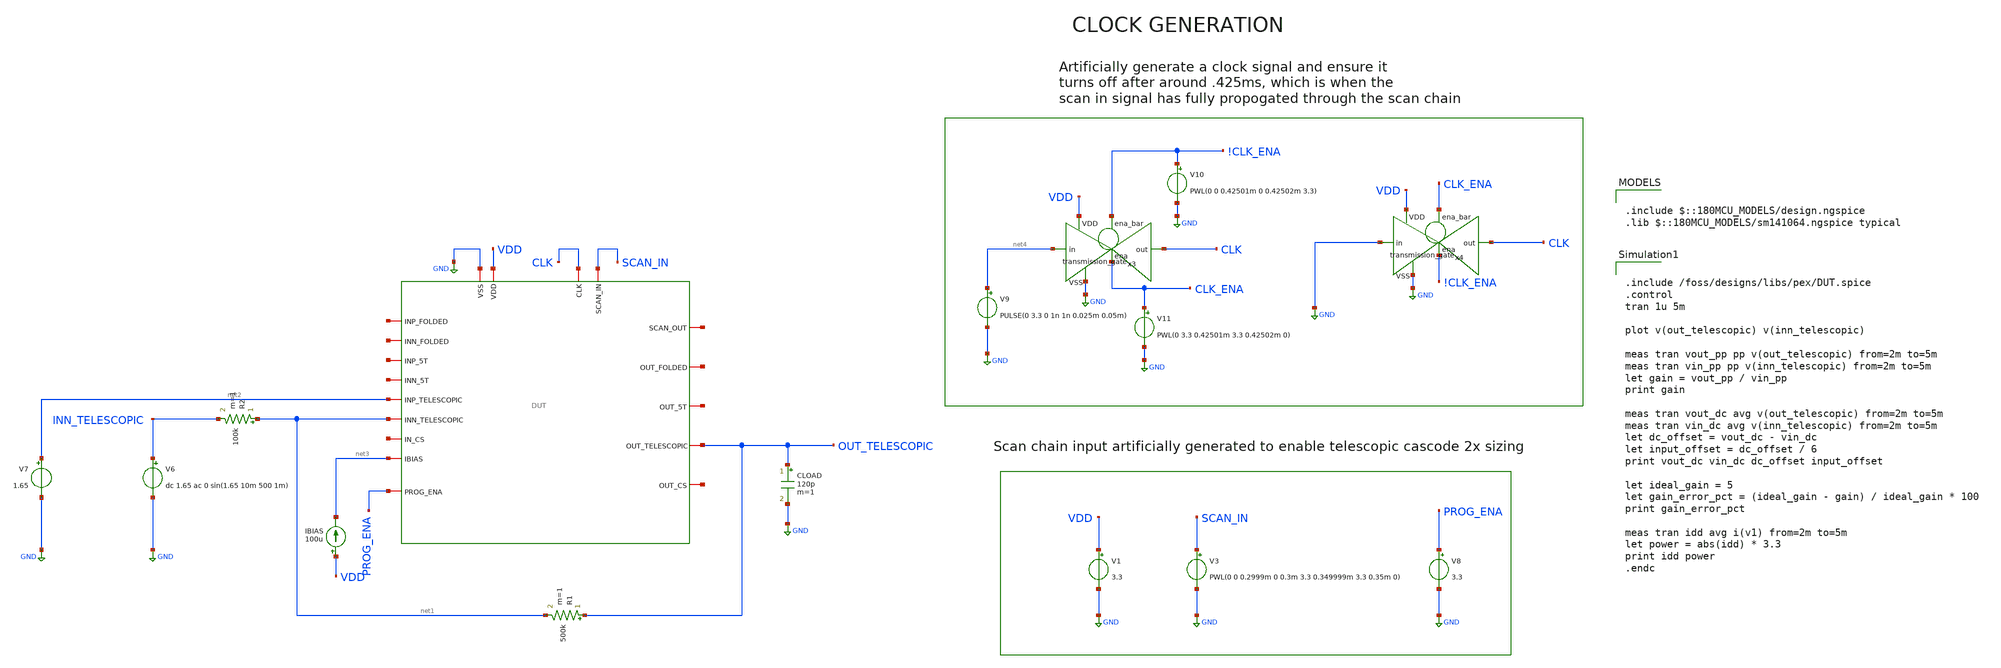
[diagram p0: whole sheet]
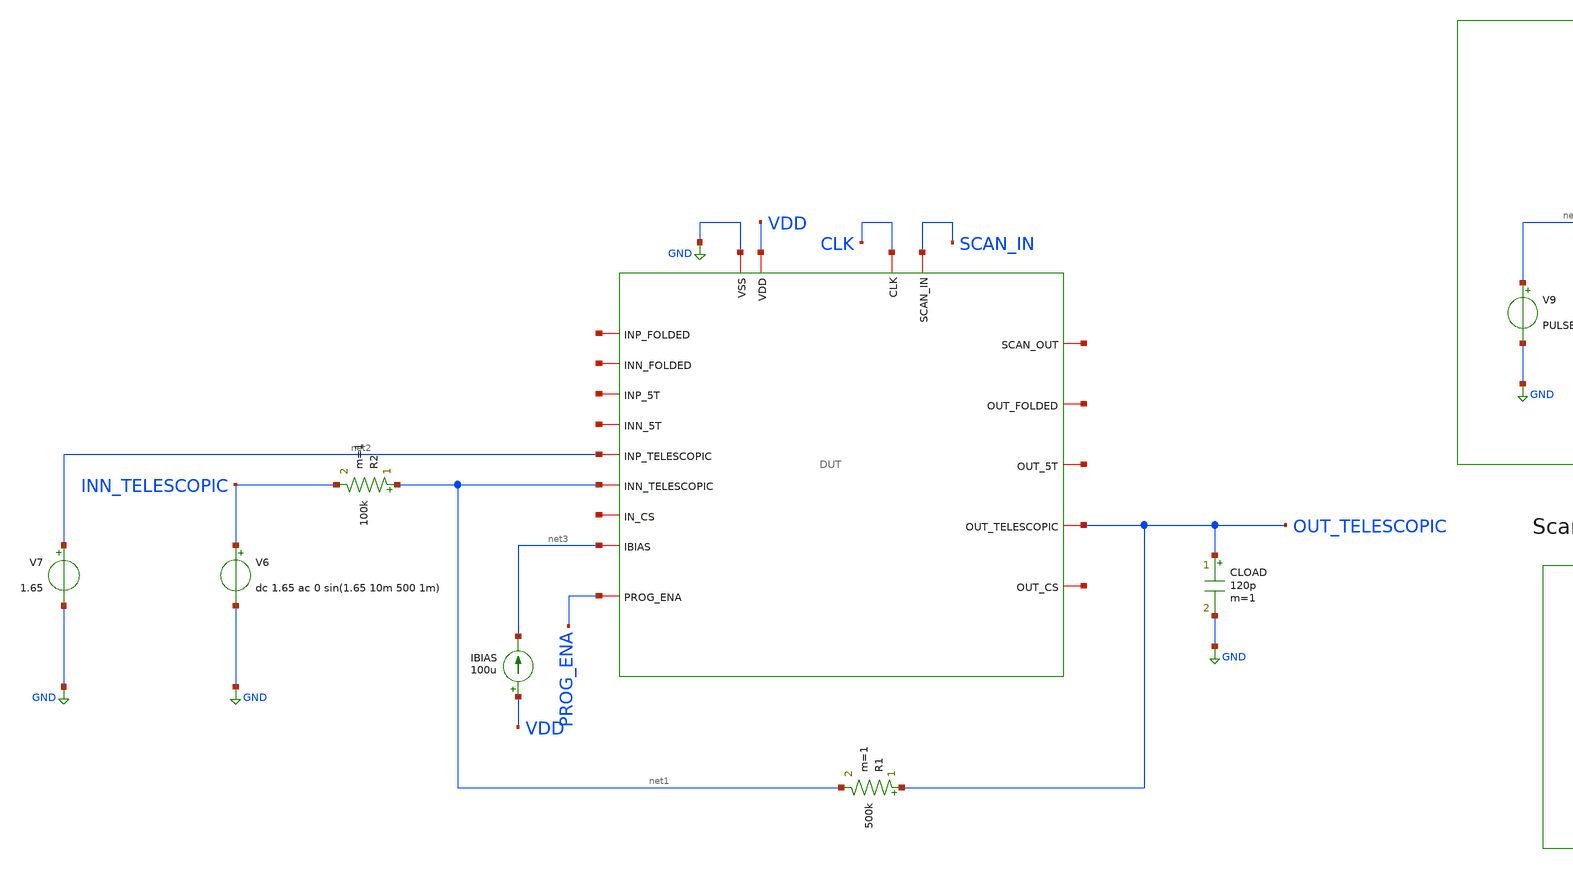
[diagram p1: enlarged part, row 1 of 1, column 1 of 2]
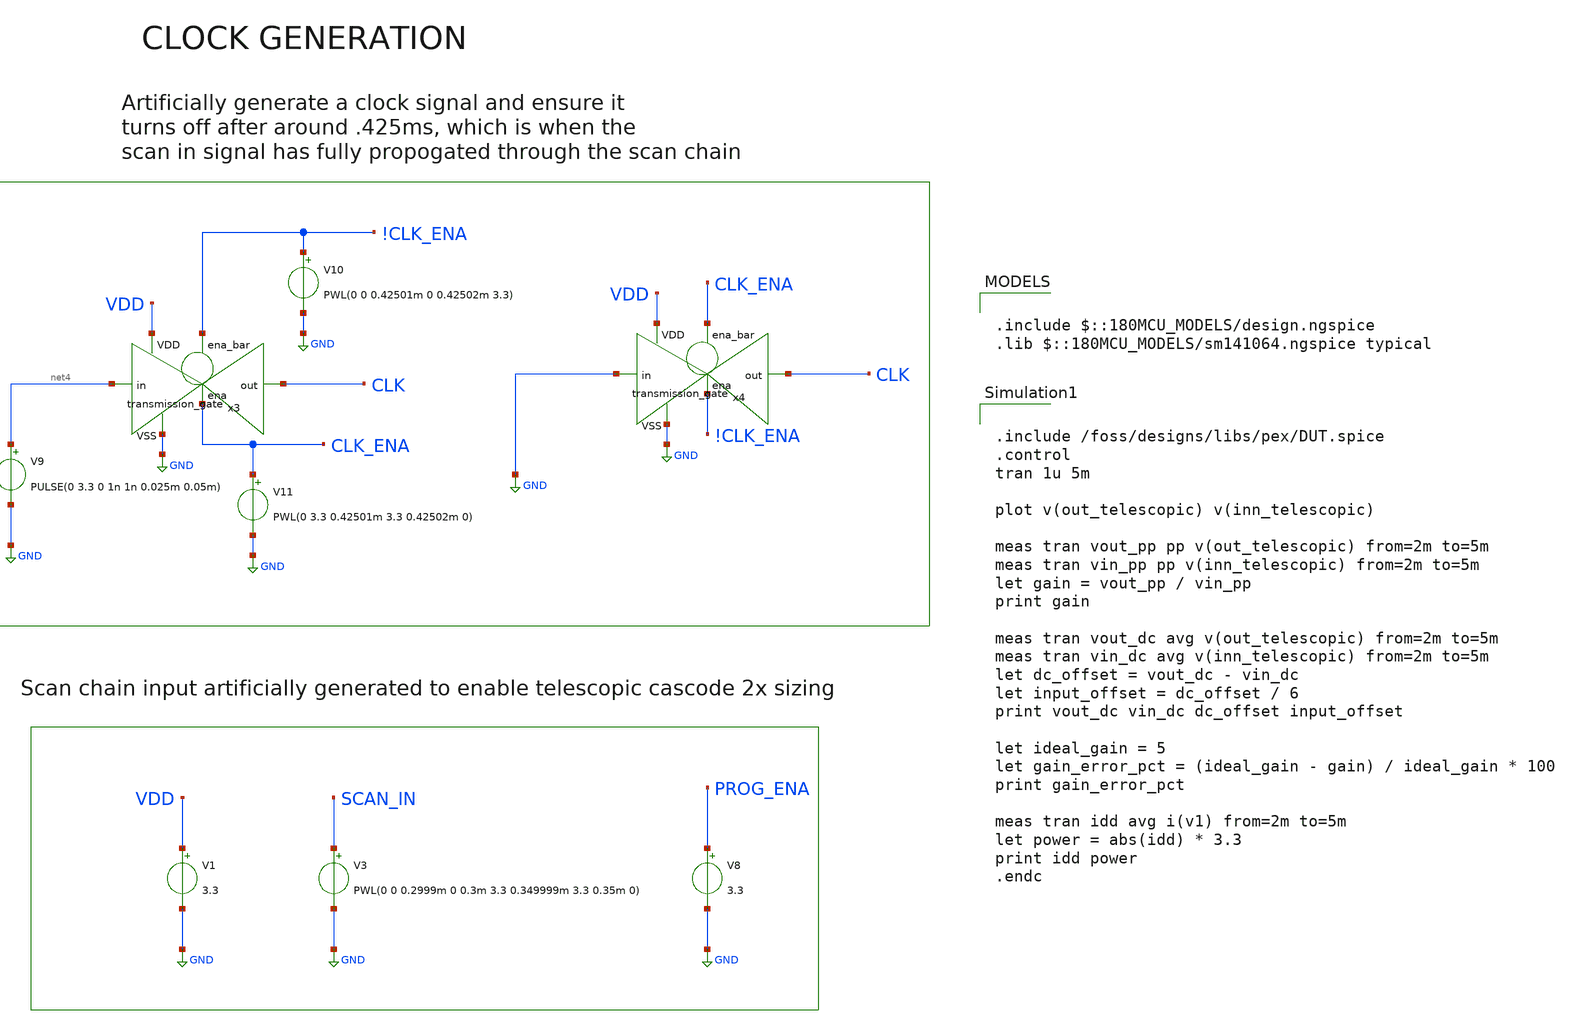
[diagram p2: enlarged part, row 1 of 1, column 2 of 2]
** sch_path: designs/libs/pex/tele/inverting_amplifier/2x.sch
**.subckt 2x
CLOAD OUT_TELESCOPIC GND 120p m=1
R1 OUT_TELESCOPIC net1 500k m=1
R2 net1 INN_TELESCOPIC 100k m=1
V6 INN_TELESCOPIC GND dc 1.65 ac 0 sin(1.65 10m 500 1m)
V7 net2 GND 1.65
IBIAS VDD net3 100u
V3 SCAN_IN GND PWL(0 0 0.2999m 0 0.3m 3.3 0.349999m 3.3 0.35m 0)
V1 VDD GND 3.3
V8 PROG_ENA GND 3.3
V9 net4 GND PULSE(0 3.3 0 1n 1n 0.025m 0.05m)
x3 !CLK_ENA VDD CLK net4 GND CLK_ENA transmission_gate
V10 !CLK_ENA GND PWL(0 0 0.42501m 0 0.42502m 3.3)
V11 CLK_ENA GND PWL(0 3.3 0.42501m 3.3 0.42502m 0)
x4 CLK_ENA VDD CLK GND GND !CLK_ENA transmission_gate
x1 CLK net5 SCAN_IN GND VDD net6 net7 net8 net3 net9 net10 net11 net2 OUT_TELESCOPIC net12 net13
+ net1 PROG_ENA DUT
**** begin user architecture code

.include $::180MCU_MODELS/design.ngspice
.lib $::180MCU_MODELS/sm141064.ngspice typical



.include /foss/designs/libs/pex/DUT.spice
.control
tran 1u 5m

plot v(out_telescopic) v(inn_telescopic)

meas tran vout_pp pp v(out_telescopic) from=2m to=5m
meas tran vin_pp pp v(inn_telescopic) from=2m to=5m
let gain = vout_pp / vin_pp
print gain

meas tran vout_dc avg v(out_telescopic) from=2m to=5m
meas tran vin_dc avg v(inn_telescopic) from=2m to=5m
let dc_offset = vout_dc - vin_dc
let input_offset = dc_offset / 6
print vout_dc vin_dc dc_offset input_offset

let ideal_gain = 5
let gain_error_pct = (ideal_gain - gain) / ideal_gain * 100
print gain_error_pct

meas tran idd avg i(v1) from=2m to=5m
let power = abs(idd) * 3.3
print idd power
.endc


**** end user architecture code
**.ends

* expanding   symbol:  libs/core_digital/schem/transmission_gate.sym # of pins=6
** sym_path: designs/libs/core_digital/schem/transmission_gate.sym
** sch_path: designs/libs/core_digital/schem/transmission_gate.sch
.subckt transmission_gate ena_bar VDD out in VSS ena
*.ipin in
*.ipin ena_bar
*.ipin ena
*.ipin VSS
*.ipin VDD
*.opin out
XM1 in ena_bar out VDD pfet_03v3 L=0.28u W=0.22u nf=1 ad='int((nf+1)/2) * W/nf * 0.18u' as='int((nf+2)/2) * W/nf * 0.18u'
+ pd='2*int((nf+1)/2) * (W/nf + 0.18u)' ps='2*int((nf+2)/2) * (W/nf + 0.18u)' nrd='0.18u / W' nrs='0.18u / W'
+ sa=0 sb=0 sd=0 m=1
XM2 in ena out VSS nfet_03v3 L=0.28u W=0.22u nf=1 ad='int((nf+1)/2) * W/nf * 0.18u' as='int((nf+2)/2) * W/nf * 0.18u'
+ pd='2*int((nf+1)/2) * (W/nf + 0.18u)' ps='2*int((nf+2)/2) * (W/nf + 0.18u)' nrd='0.18u / W' nrs='0.18u / W'
+ sa=0 sb=0 sd=0 m=1
.ends

.GLOBAL GND
.end
